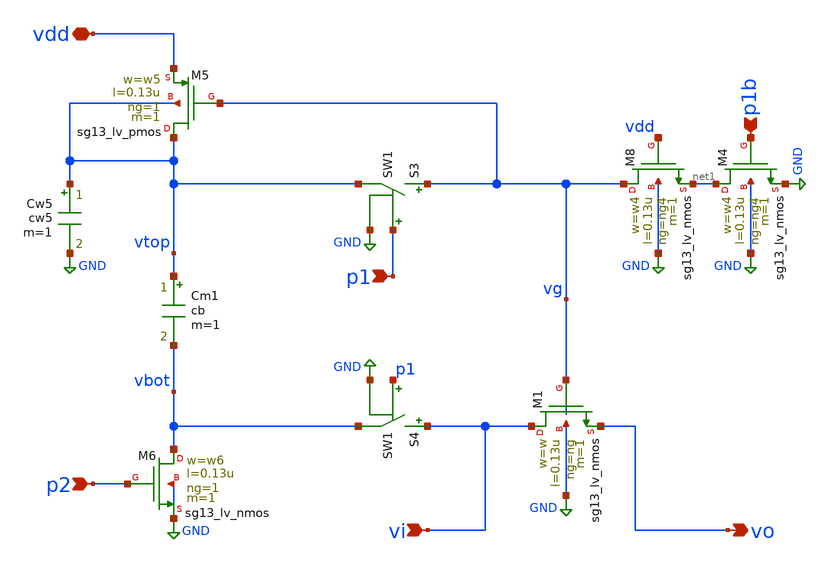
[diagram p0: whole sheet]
** sch_path: xschem/boot3.sch
**.subckt boot3 vi vo p2 vdd p1 p1b
*.ipin vi
*.opin vo
*.ipin p2
*.iopin vdd
*.ipin p1
*.ipin p1b
Cm1 vtop vbot cb m=1
S4 vi vbot p1 GND SW1
XM1 vi vg vo GND sg13_lv_nmos w=w l=0.13u ng=ng m=1 mm_ok=1
XM8 vg vdd net1 GND sg13_lv_nmos w=w4 l=0.13u ng=ng4 m=1 mm_ok=1
XM4 net1 p1b GND GND sg13_lv_nmos w=w4 l=0.13u ng=ng4 m=1 mm_ok=1
XM6 vbot p2 GND GND sg13_lv_nmos w=w6 l=0.13u ng=1 m=1 mm_ok=1
XM5 vtop vg vdd vtop sg13_lv_pmos w=w5 l=0.13u ng=1 m=1 mm_ok=1
S3 vg vtop p1 GND SW1
Cw5 vtop GND cw5 m=1
**.ends
.GLOBAL GND
**** begin user architecture code
.MODEL SW1 SW   VT=0.6 VH=vh  RON=rsw ROFF=roff
**** end user architecture code
.end
